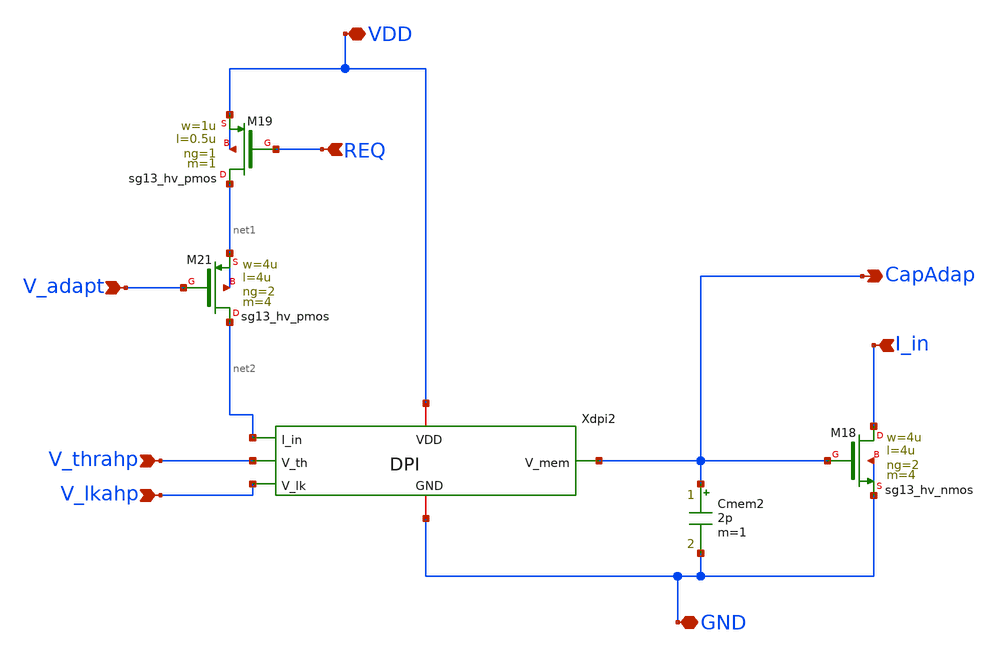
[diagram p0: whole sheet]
** sch_path: xschem/ADAP_system.sch
**.subckt ADAP_system VDD GND REQ V_adapt V_thrahp V_lkahp I_in CapAdap
*.iopin VDD
*.iopin GND
*.ipin REQ
*.ipin V_adapt
*.ipin V_thrahp
*.ipin V_lkahp
*.ipin I_in
*.opin CapAdap
XM19 net1 REQ VDD VDD sg13_hv_pmos w=1u l=0.5u ng=1 m=1 mm_ok=1
XM21 net2 V_adapt net1 net1 sg13_hv_pmos w=4u l=4u ng=2 m=4 mm_ok=1
XM18 I_in CapAdap GND GND sg13_hv_nmos w=4u l=4u ng=2 m=4 mm_ok=1
Cmem2 CapAdap GND 2p m=1
Xdpi2 net2 VDD V_thrahp CapAdap V_lkahp GND DPI
**.ends

* expanding   symbol:  DPI.sym # of pins=6
** sym_path: DPI.sym
** sch_path: DPI.sch
.subckt DPI I_in VDD V_th V_mem V_lk GND
*.opin V_mem
*.ipin V_lk
*.ipin V_th
*.ipin I_in
*.iopin VDD
*.iopin GND
XM24 GND V_th I_in VDD sg13_hv_pmos w=4u l=8u ng=1 m=4 mm_ok=1
XM25 V_mem V_mem I_in VDD sg13_hv_pmos w=4u l=8u ng=1 m=4 mm_ok=1
XM28 V_mem V_lk GND GND sg13_hv_nmos w=4u l=10u ng=1 m=4 mm_ok=1
.ends

.end
